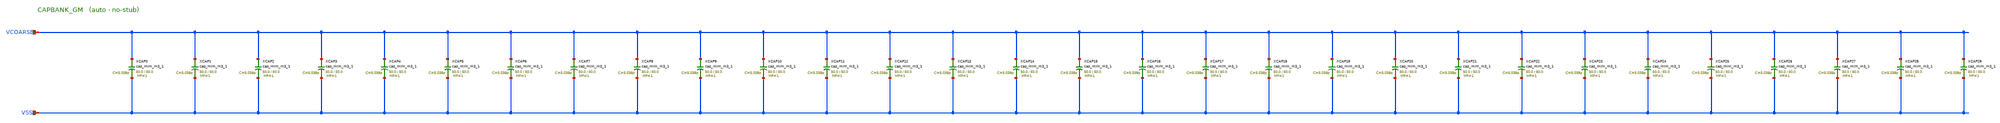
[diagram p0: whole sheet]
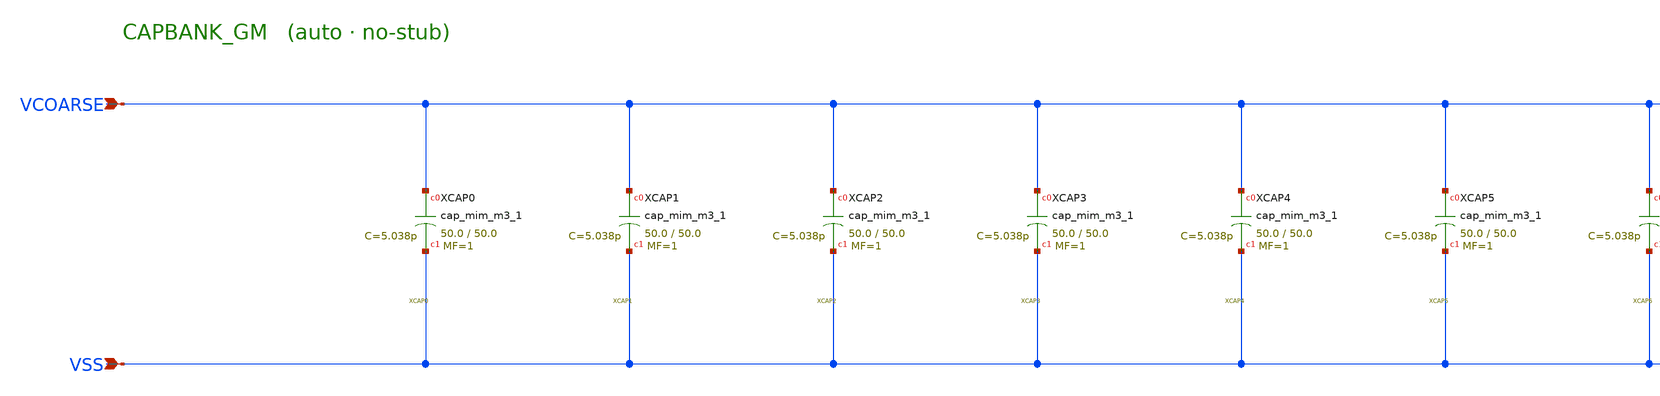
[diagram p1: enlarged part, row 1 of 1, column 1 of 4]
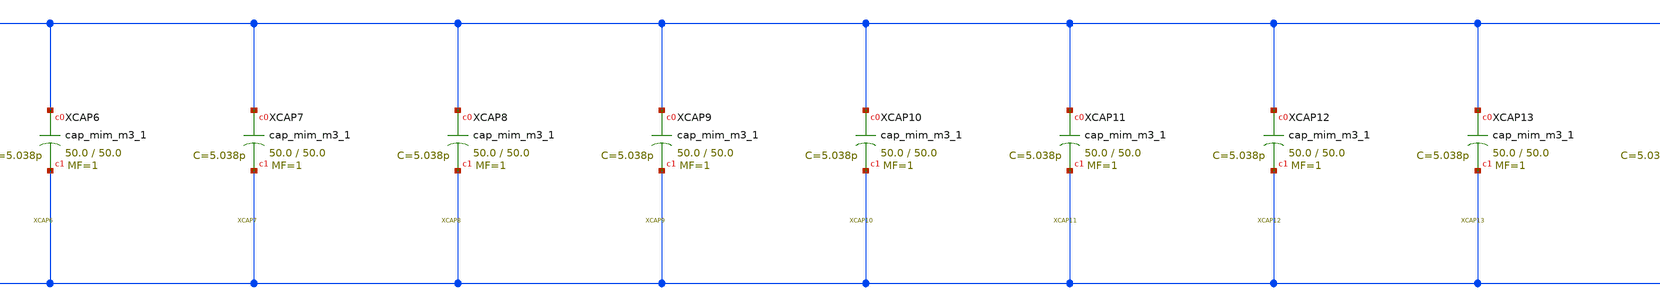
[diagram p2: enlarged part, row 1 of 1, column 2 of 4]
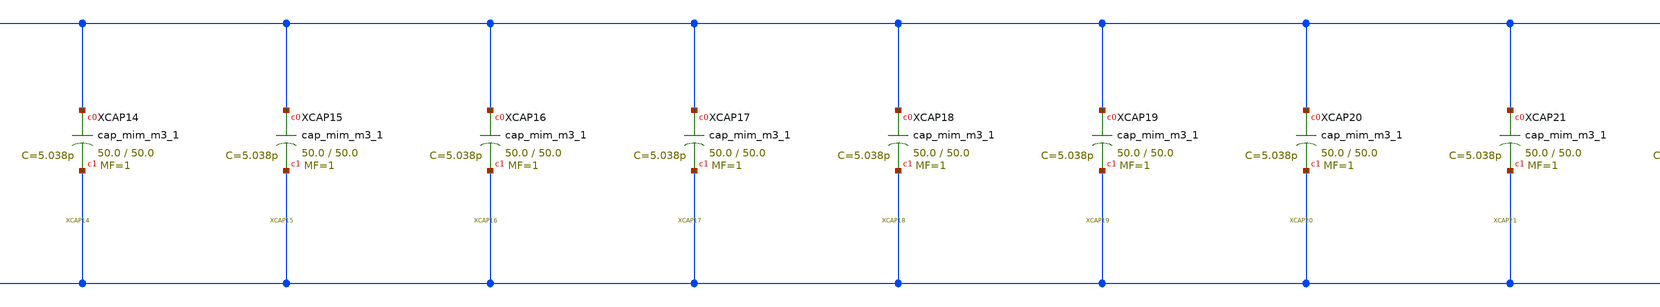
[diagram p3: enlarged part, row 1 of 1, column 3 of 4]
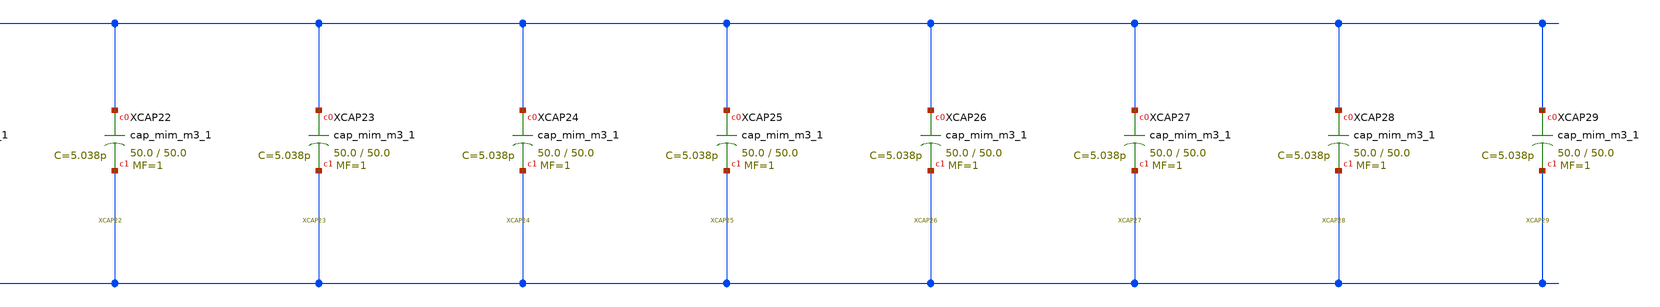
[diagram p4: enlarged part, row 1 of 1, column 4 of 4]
** sch_path: schematics/CAPBANK_GM.sch
**.subckt CAPBANK_GM VSS VCOARSE
*.ipin VSS
*.ipin VCOARSE
XXCAP0 VCOARSE VSS sky130_fd_pr__cap_mim_m3_1 W=50.0 L=50.0 MF=1 m=1
XXCAP1 VCOARSE VSS sky130_fd_pr__cap_mim_m3_1 W=50.0 L=50.0 MF=1 m=1
XXCAP2 VCOARSE VSS sky130_fd_pr__cap_mim_m3_1 W=50.0 L=50.0 MF=1 m=1
XXCAP3 VCOARSE VSS sky130_fd_pr__cap_mim_m3_1 W=50.0 L=50.0 MF=1 m=1
XXCAP4 VCOARSE VSS sky130_fd_pr__cap_mim_m3_1 W=50.0 L=50.0 MF=1 m=1
XXCAP5 VCOARSE VSS sky130_fd_pr__cap_mim_m3_1 W=50.0 L=50.0 MF=1 m=1
XXCAP6 VCOARSE VSS sky130_fd_pr__cap_mim_m3_1 W=50.0 L=50.0 MF=1 m=1
XXCAP7 VCOARSE VSS sky130_fd_pr__cap_mim_m3_1 W=50.0 L=50.0 MF=1 m=1
XXCAP8 VCOARSE VSS sky130_fd_pr__cap_mim_m3_1 W=50.0 L=50.0 MF=1 m=1
XXCAP9 VCOARSE VSS sky130_fd_pr__cap_mim_m3_1 W=50.0 L=50.0 MF=1 m=1
XXCAP10 VCOARSE VSS sky130_fd_pr__cap_mim_m3_1 W=50.0 L=50.0 MF=1 m=1
XXCAP11 VCOARSE VSS sky130_fd_pr__cap_mim_m3_1 W=50.0 L=50.0 MF=1 m=1
XXCAP12 VCOARSE VSS sky130_fd_pr__cap_mim_m3_1 W=50.0 L=50.0 MF=1 m=1
XXCAP13 VCOARSE VSS sky130_fd_pr__cap_mim_m3_1 W=50.0 L=50.0 MF=1 m=1
XXCAP14 VCOARSE VSS sky130_fd_pr__cap_mim_m3_1 W=50.0 L=50.0 MF=1 m=1
XXCAP15 VCOARSE VSS sky130_fd_pr__cap_mim_m3_1 W=50.0 L=50.0 MF=1 m=1
XXCAP16 VCOARSE VSS sky130_fd_pr__cap_mim_m3_1 W=50.0 L=50.0 MF=1 m=1
XXCAP17 VCOARSE VSS sky130_fd_pr__cap_mim_m3_1 W=50.0 L=50.0 MF=1 m=1
XXCAP18 VCOARSE VSS sky130_fd_pr__cap_mim_m3_1 W=50.0 L=50.0 MF=1 m=1
XXCAP19 VCOARSE VSS sky130_fd_pr__cap_mim_m3_1 W=50.0 L=50.0 MF=1 m=1
XXCAP20 VCOARSE VSS sky130_fd_pr__cap_mim_m3_1 W=50.0 L=50.0 MF=1 m=1
XXCAP21 VCOARSE VSS sky130_fd_pr__cap_mim_m3_1 W=50.0 L=50.0 MF=1 m=1
XXCAP22 VCOARSE VSS sky130_fd_pr__cap_mim_m3_1 W=50.0 L=50.0 MF=1 m=1
XXCAP23 VCOARSE VSS sky130_fd_pr__cap_mim_m3_1 W=50.0 L=50.0 MF=1 m=1
XXCAP24 VCOARSE VSS sky130_fd_pr__cap_mim_m3_1 W=50.0 L=50.0 MF=1 m=1
XXCAP25 VCOARSE VSS sky130_fd_pr__cap_mim_m3_1 W=50.0 L=50.0 MF=1 m=1
XXCAP26 VCOARSE VSS sky130_fd_pr__cap_mim_m3_1 W=50.0 L=50.0 MF=1 m=1
XXCAP27 VCOARSE VSS sky130_fd_pr__cap_mim_m3_1 W=50.0 L=50.0 MF=1 m=1
XXCAP28 VCOARSE VSS sky130_fd_pr__cap_mim_m3_1 W=50.0 L=50.0 MF=1 m=1
XXCAP29 VCOARSE VSS sky130_fd_pr__cap_mim_m3_1 W=50.0 L=50.0 MF=1 m=1
**.ends
.end
